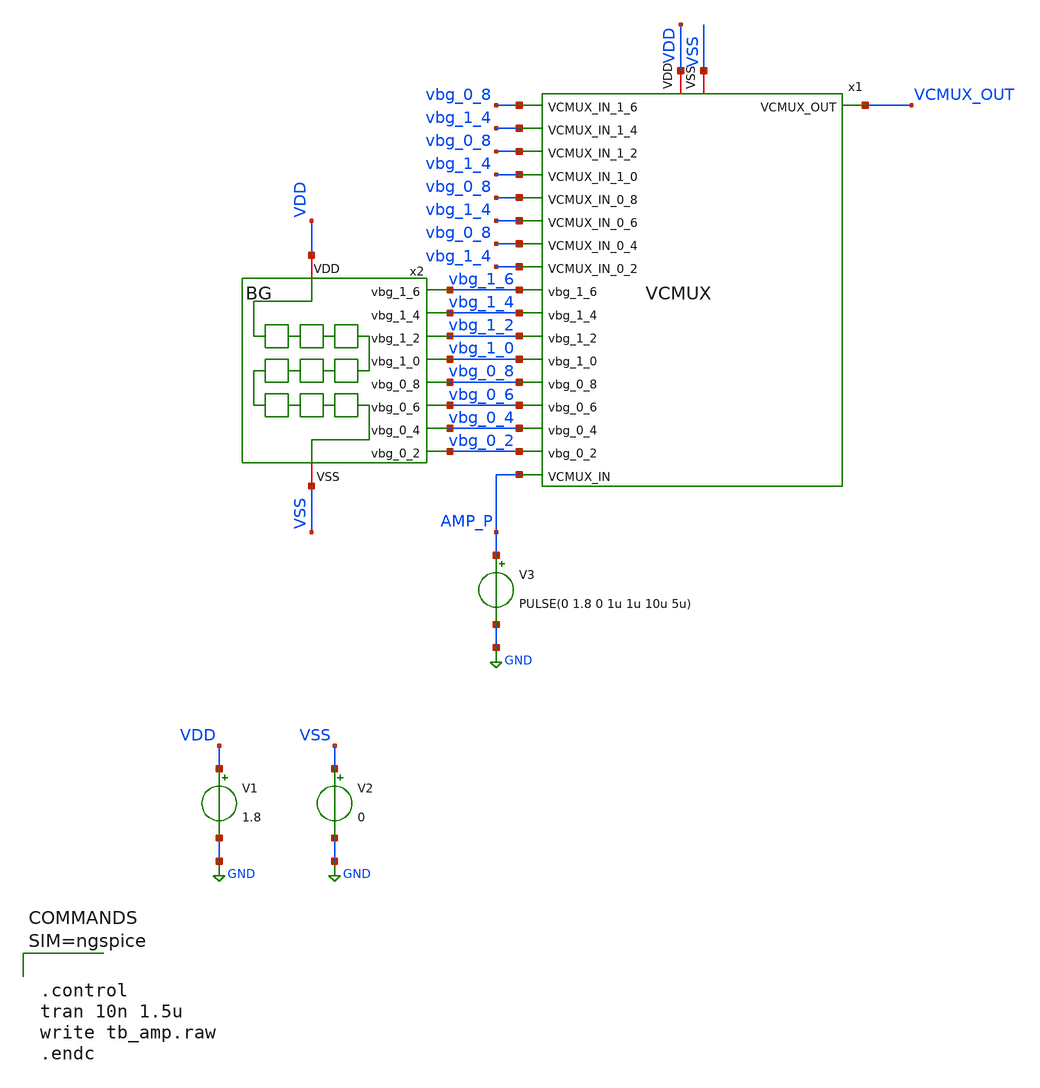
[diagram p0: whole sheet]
** sch_path: xschem/tb_amp.sch
**.subckt tb_amp
V1 VDD GND 1.8
V2 VSS GND 0
x2 vbg_1_6 vbg_1_4 vbg_1_2 vbg_1_0 vbg_0_8 vbg_0_6 vbg_0_4 vbg_0_2 VDD VSS BG
V3 AMP_P GND PULSE(0 1.8 0 1u 1u 10u 5u)
x1 vbg_0_8 VCMUX_OUT vbg_1_4 vbg_0_8 vbg_1_4 vbg_0_8 vbg_1_4 vbg_0_8 vbg_1_4 vbg_1_6 VDD vbg_1_4 VSS
+ vbg_1_2 vbg_1_0 vbg_0_8 vbg_0_6 vbg_0_4 vbg_0_2 AMP_P VCMUX
**** begin user architecture code

** opencircuitdesign pdks install
.lib $::SKYWATER_MODELS/sky130.lib.spice tt





.control
tran 10n 1.5u
write tb_amp.raw
.endc



**** end user architecture code
**.ends
.GLOBAL GND
.end
